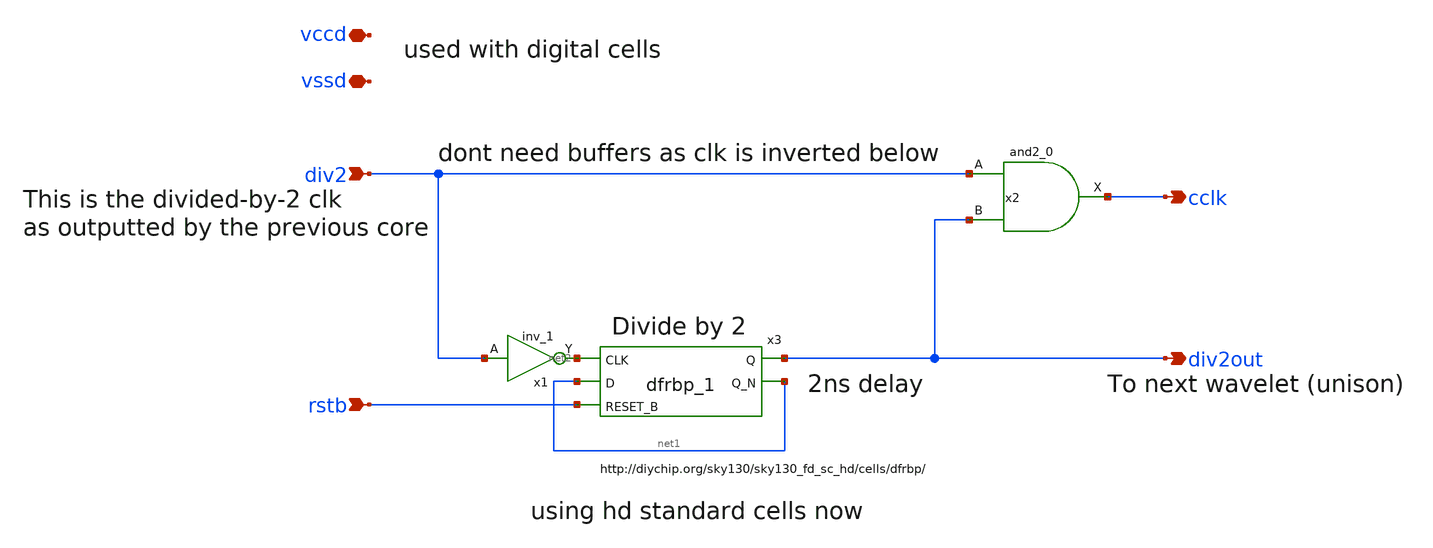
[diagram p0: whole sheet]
** sch_path: xschem/digital/dig_div2.sch
**.subckt dig_div2 div2 rstb cclk div2out vccd vssd
*.ipin div2
*.ipin rstb
*.opin cclk
*.opin div2out
*.iopin vccd
*.iopin vssd
x3 net2 net1 rstb vssd vssd vccd vccd div2out net1 sky130_fd_sc_hd__dfrbp_1
x2 div2 div2out vssd vssd vccd vccd cclk sky130_fd_sc_hd__and2_0
x1 div2 vssd vssd vccd vccd net2 sky130_fd_sc_hd__inv_1
**.ends
.end
